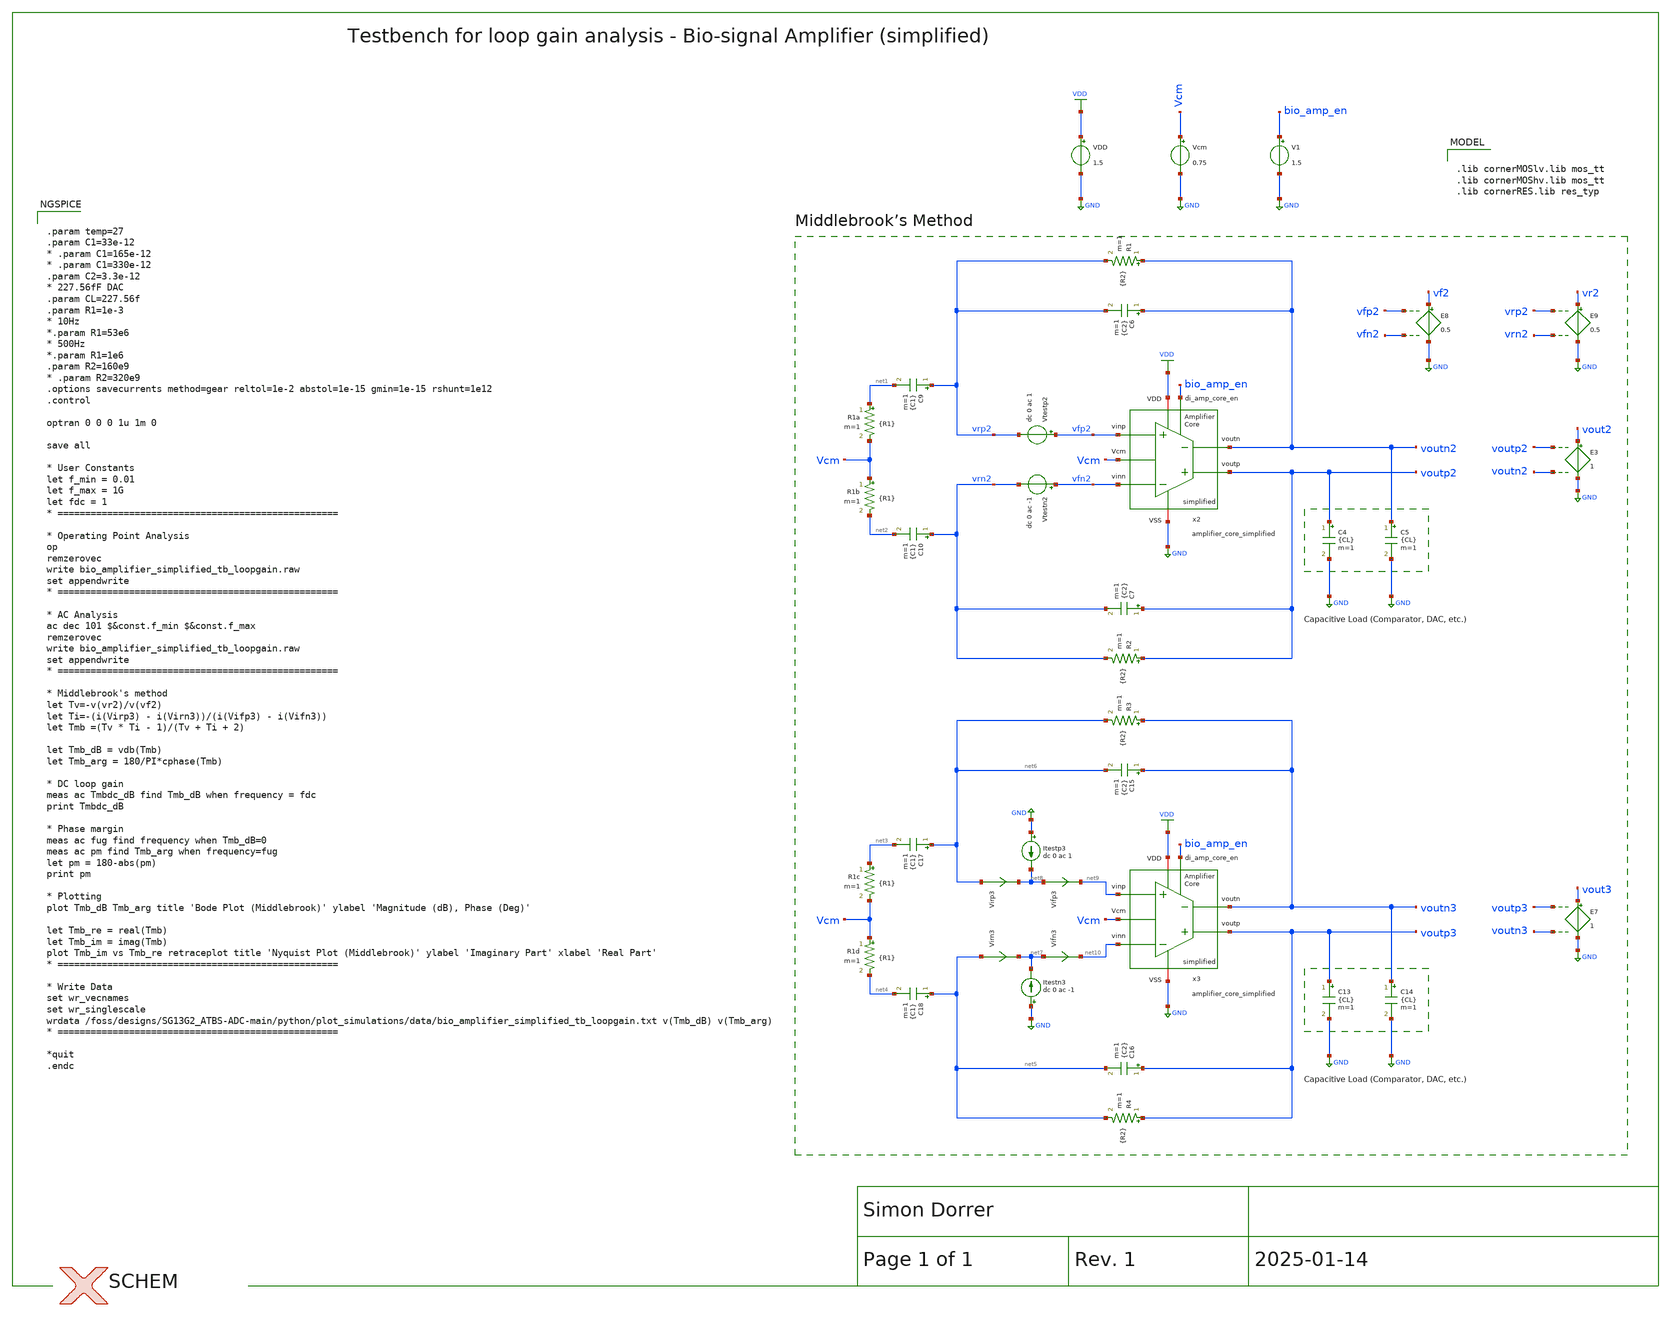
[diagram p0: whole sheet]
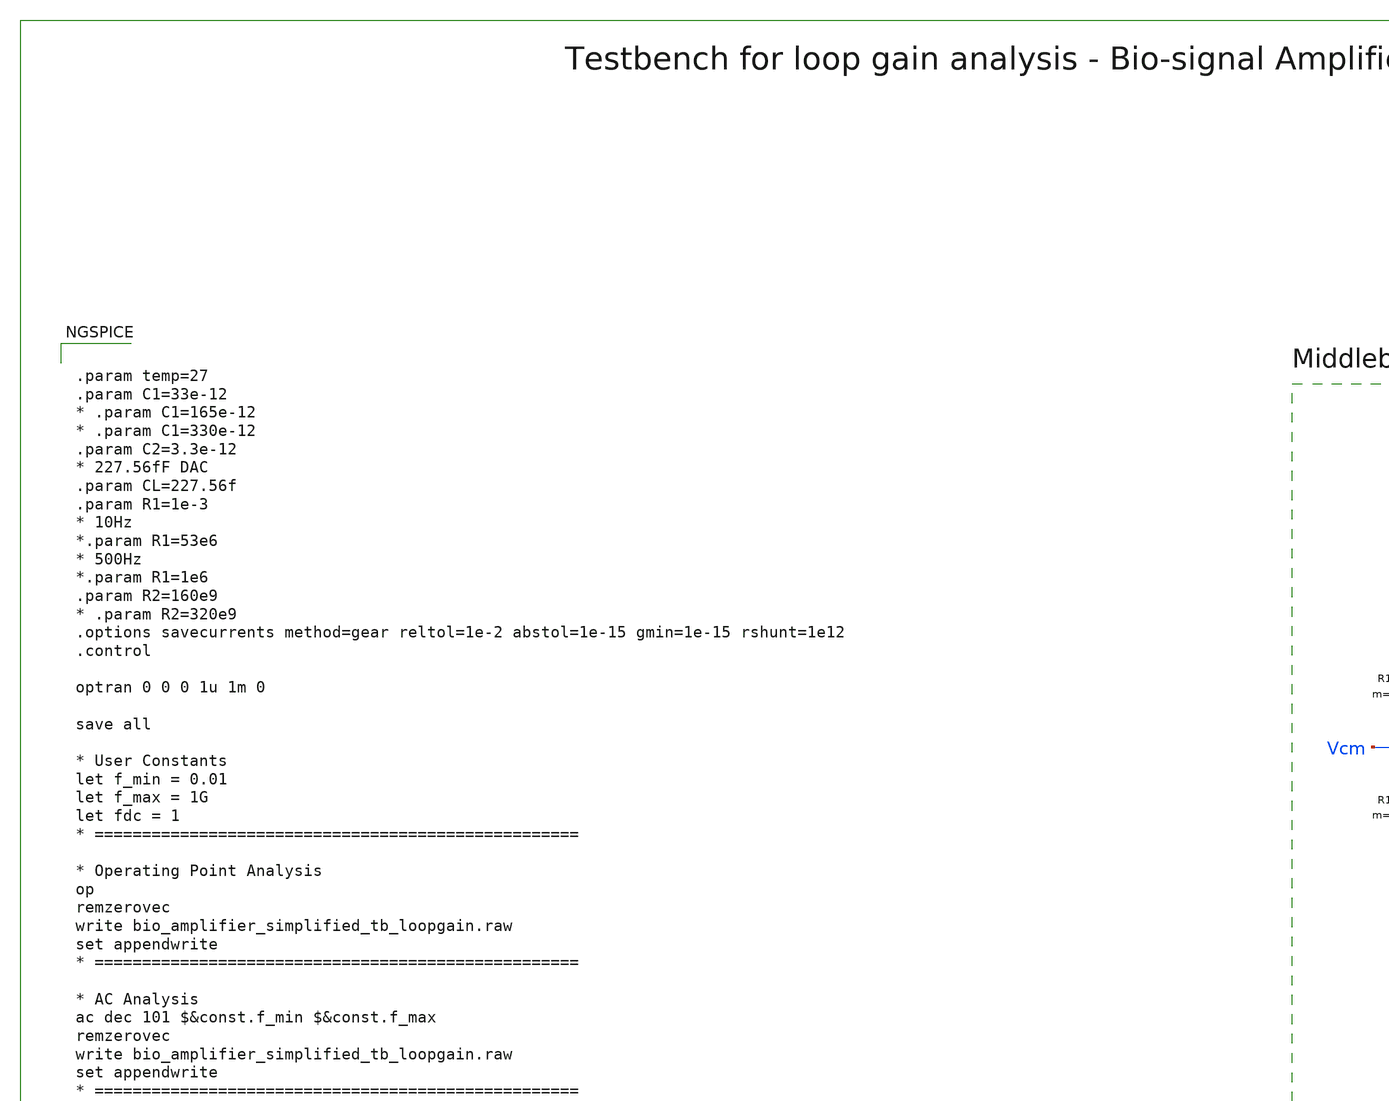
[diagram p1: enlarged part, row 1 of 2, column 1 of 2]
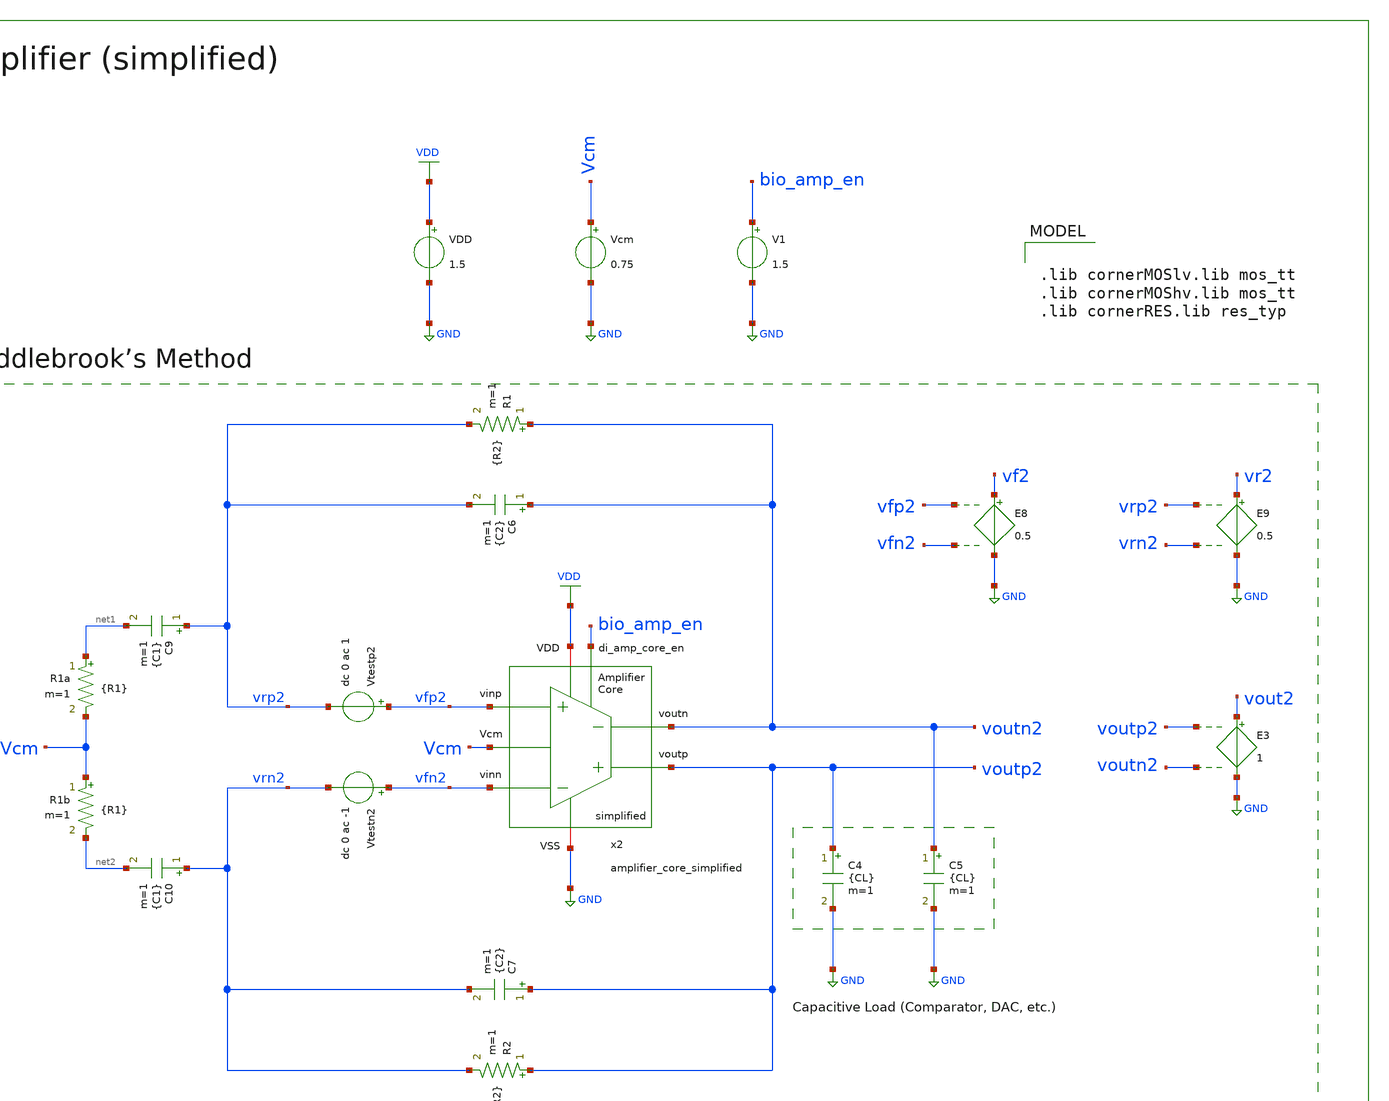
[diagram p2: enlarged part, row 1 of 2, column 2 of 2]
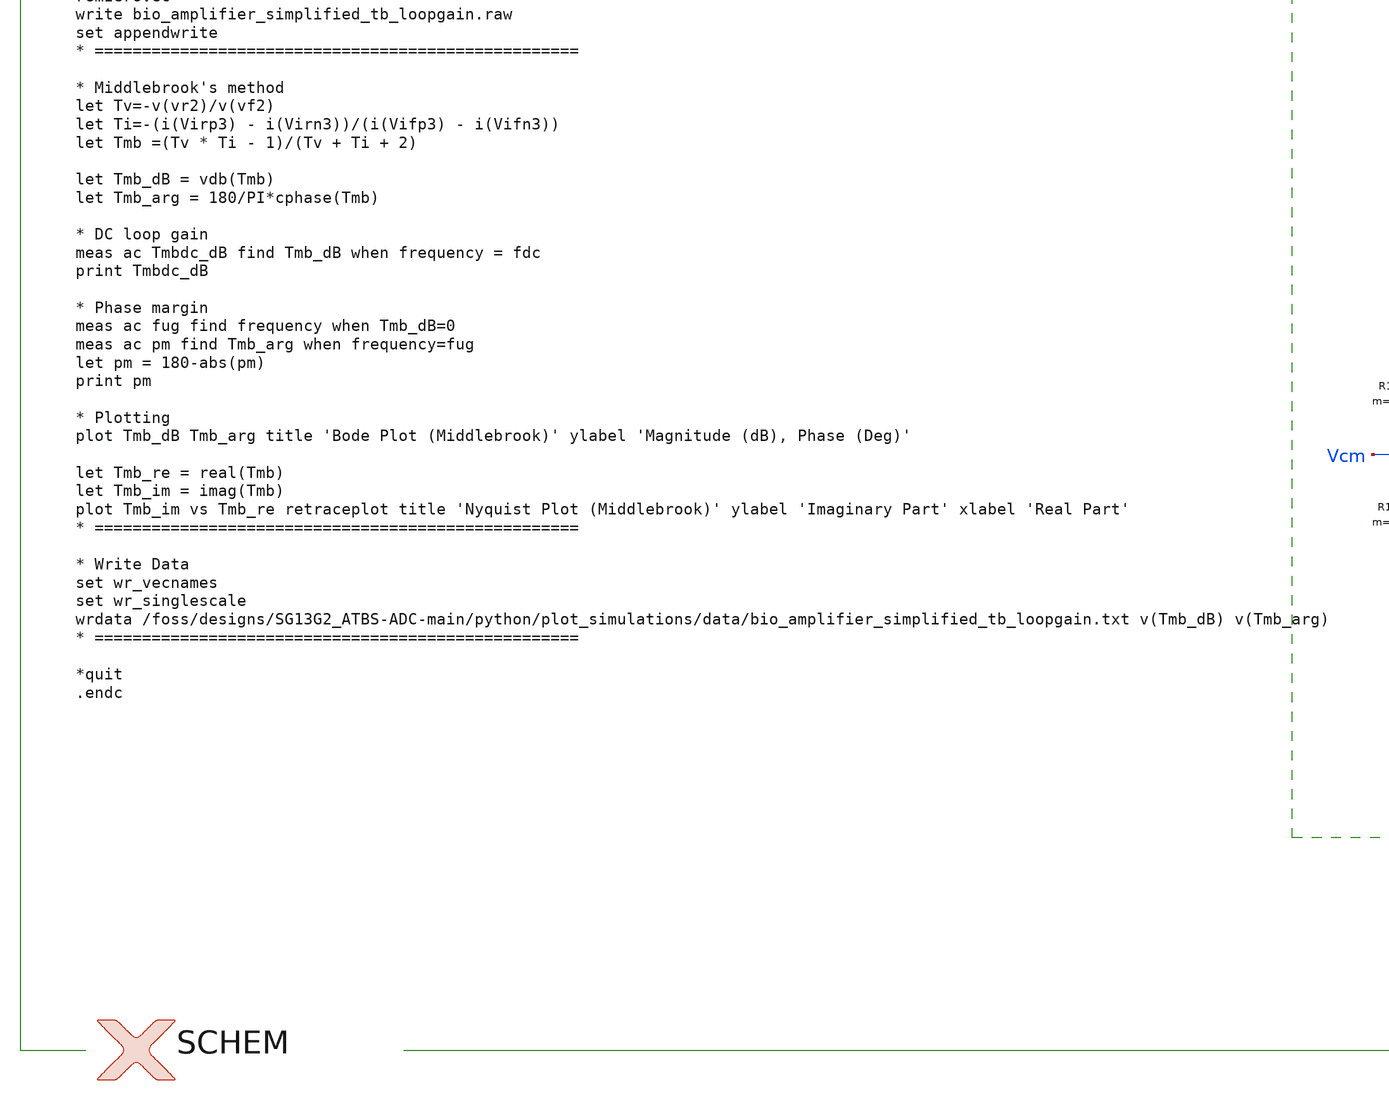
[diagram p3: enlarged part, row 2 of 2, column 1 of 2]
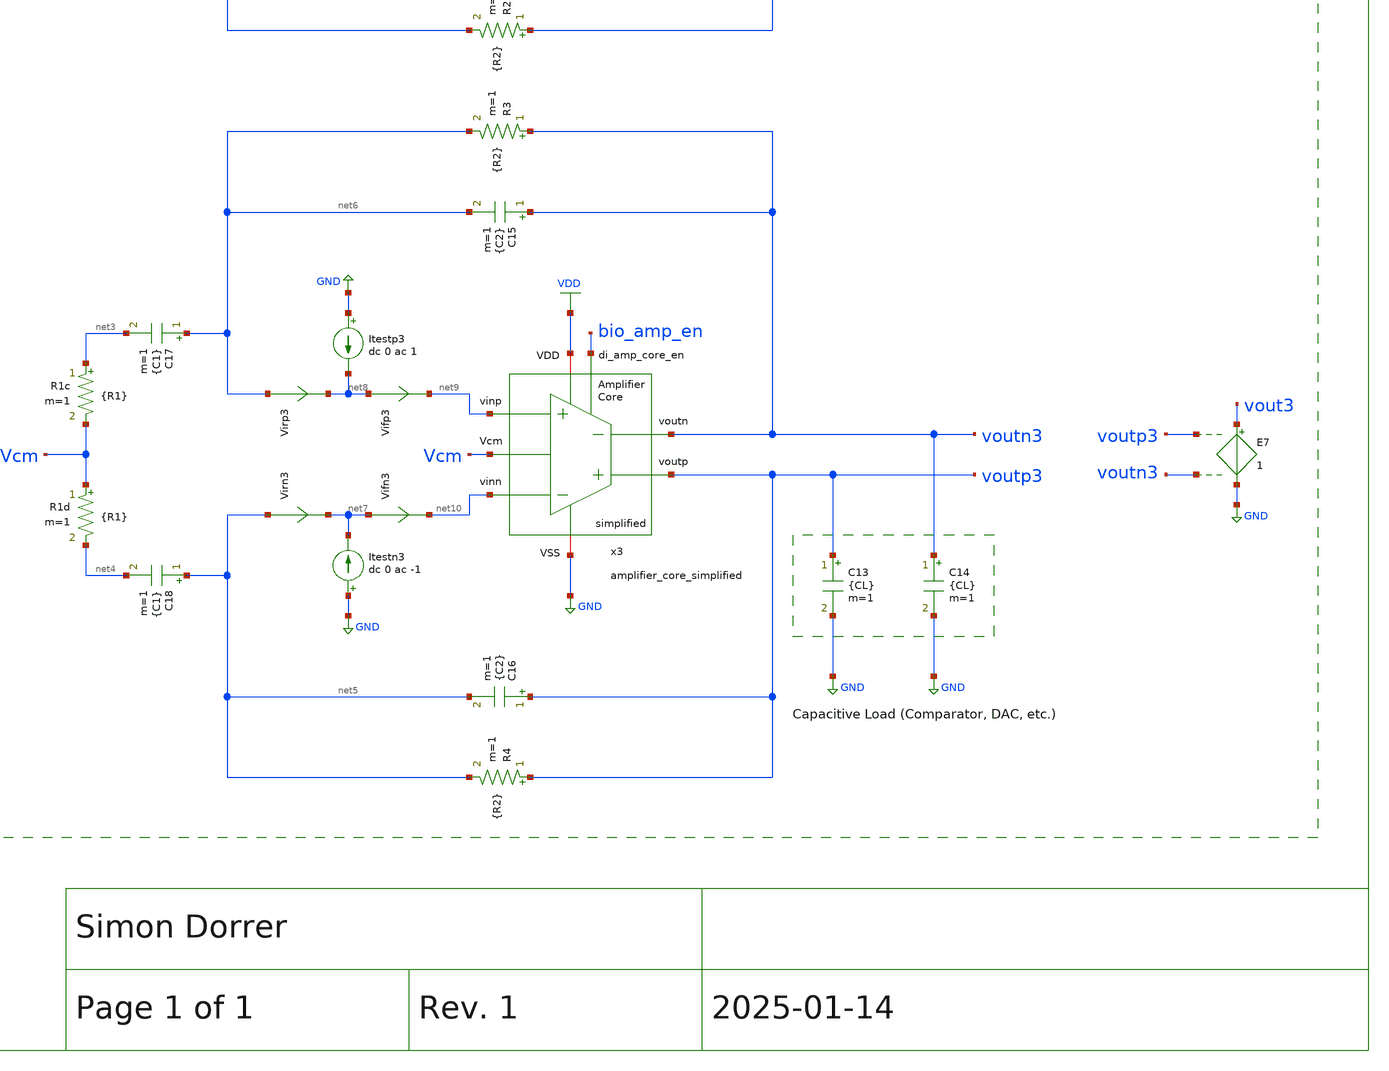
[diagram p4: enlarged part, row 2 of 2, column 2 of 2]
** sch_path: SG13G2_ATBS-ADC-main/xschem/bio_amplifier/testbenches/bio_amplifier_simplified_tb_loopgain.sch
**.subckt bio_amplifier_simplified_tb_loopgain
VDD VDD GND 1.5
V1 bio_amp_en GND 1.5
C4 voutp2 GND {CL} m=1
C5 voutn2 GND {CL} m=1
E3 vout2 GND voutp2 voutn2 1
R1 voutn2 vrp2 {R2} m=1
R2 voutp2 vrn2 {R2} m=1
x2 voutp2 voutn2 bio_amp_en vfn2 vfp2 VDD GND Vcm amplifier_core_simplified
C6 voutn2 vrp2 {C2} m=1
C7 voutp2 vrn2 {C2} m=1
C9 vrp2 net1 {C1} m=1
C10 vrn2 net2 {C1} m=1
C13 voutp3 GND {CL} m=1
C14 voutn3 GND {CL} m=1
E7 vout3 GND voutp3 voutn3 1
R3 voutn3 net6 {R2} m=1
R4 voutp3 net5 {R2} m=1
x3 voutp3 voutn3 bio_amp_en net10 net9 VDD GND Vcm amplifier_core_simplified
C15 voutn3 net6 {C2} m=1
C16 voutp3 net5 {C2} m=1
C17 net6 net3 {C1} m=1
C18 net5 net4 {C1} m=1
E8 vf2 GND vfp2 vfn2 0.5
E9 vr2 GND vrp2 vrn2 0.5
Vtestp2 vfp2 vrp2 dc 0 ac 1
Vtestn2 vfn2 vrn2 dc 0 ac -1
Virp3 net6 net8 0
.save i(virp3)
Vifp3 net8 net9 0
.save i(vifp3)
Itestn3 GND net7 dc 0 ac -1
Virn3 net5 net7 0
.save i(virn3)
Vifn3 net7 net10 0
.save i(vifn3)
Itestp3 GND net8 dc 0 ac 1
Vcm Vcm GND 0.75
R1a net1 Vcm {R1} m=1
R1b Vcm net2 {R1} m=1
R1c net3 Vcm {R1} m=1
R1d Vcm net4 {R1} m=1
**** begin user architecture code

.lib cornerMOSlv.lib mos_tt
.lib cornerMOShv.lib mos_tt
.lib cornerRES.lib res_typ



.param temp=27
.param C1=33e-12
* .param C1=165e-12
* .param C1=330e-12
.param C2=3.3e-12
* 227.56fF DAC
.param CL=227.56f
.param R1=1e-3
* 10Hz
*.param R1=53e6
* 500Hz
*.param R1=1e6
.param R2=160e9
* .param R2=320e9
.options savecurrents method=gear reltol=1e-2 abstol=1e-15 gmin=1e-15 rshunt=1e12
.control

optran 0 0 0 1u 1m 0

save all

* User Constants
let f_min = 0.01
let f_max = 1G
let fdc = 1
* ===================================================

* Operating Point Analysis
op
remzerovec
write bio_amplifier_simplified_tb_loopgain.raw
set appendwrite
* ===================================================

* AC Analysis
ac dec 101 $&const.f_min $&const.f_max
remzerovec
write bio_amplifier_simplified_tb_loopgain.raw
set appendwrite
* ===================================================

* Middlebrook's method
let Tv=-v(vr2)/v(vf2)
let Ti=-(i(Virp3) - i(Virn3))/(i(Vifp3) - i(Vifn3))
let Tmb =(Tv * Ti - 1)/(Tv + Ti + 2)

let Tmb_dB = vdb(Tmb)
let Tmb_arg = 180/PI*cphase(Tmb)

* DC loop gain
meas ac Tmbdc_dB find Tmb_dB when frequency = fdc
print Tmbdc_dB

* Phase margin
meas ac fug find frequency when Tmb_dB=0
meas ac pm find Tmb_arg when frequency=fug
let pm = 180-abs(pm)
print pm

* Plotting
plot Tmb_dB Tmb_arg title 'Bode Plot (Middlebrook)' ylabel 'Magnitude (dB), Phase (Deg)'

let Tmb_re = real(Tmb)
let Tmb_im = imag(Tmb)
plot Tmb_im vs Tmb_re retraceplot title 'Nyquist Plot (Middlebrook)' ylabel 'Imaginary Part' xlabel 'Real
+ Part'
* ===================================================

* Write Data
set wr_vecnames
set wr_singlescale
wrdata /foss/designs/SG13G2_ATBS-ADC-main/python/plot_simulations/data/bio_amplifier_simplified_tb_loopgain.txt v(Tmb_dB) v(Tmb_arg)
* ===================================================

*quit
.endc


**** end user architecture code
**.ends
.GLOBAL GND
.GLOBAL VDD
.end
